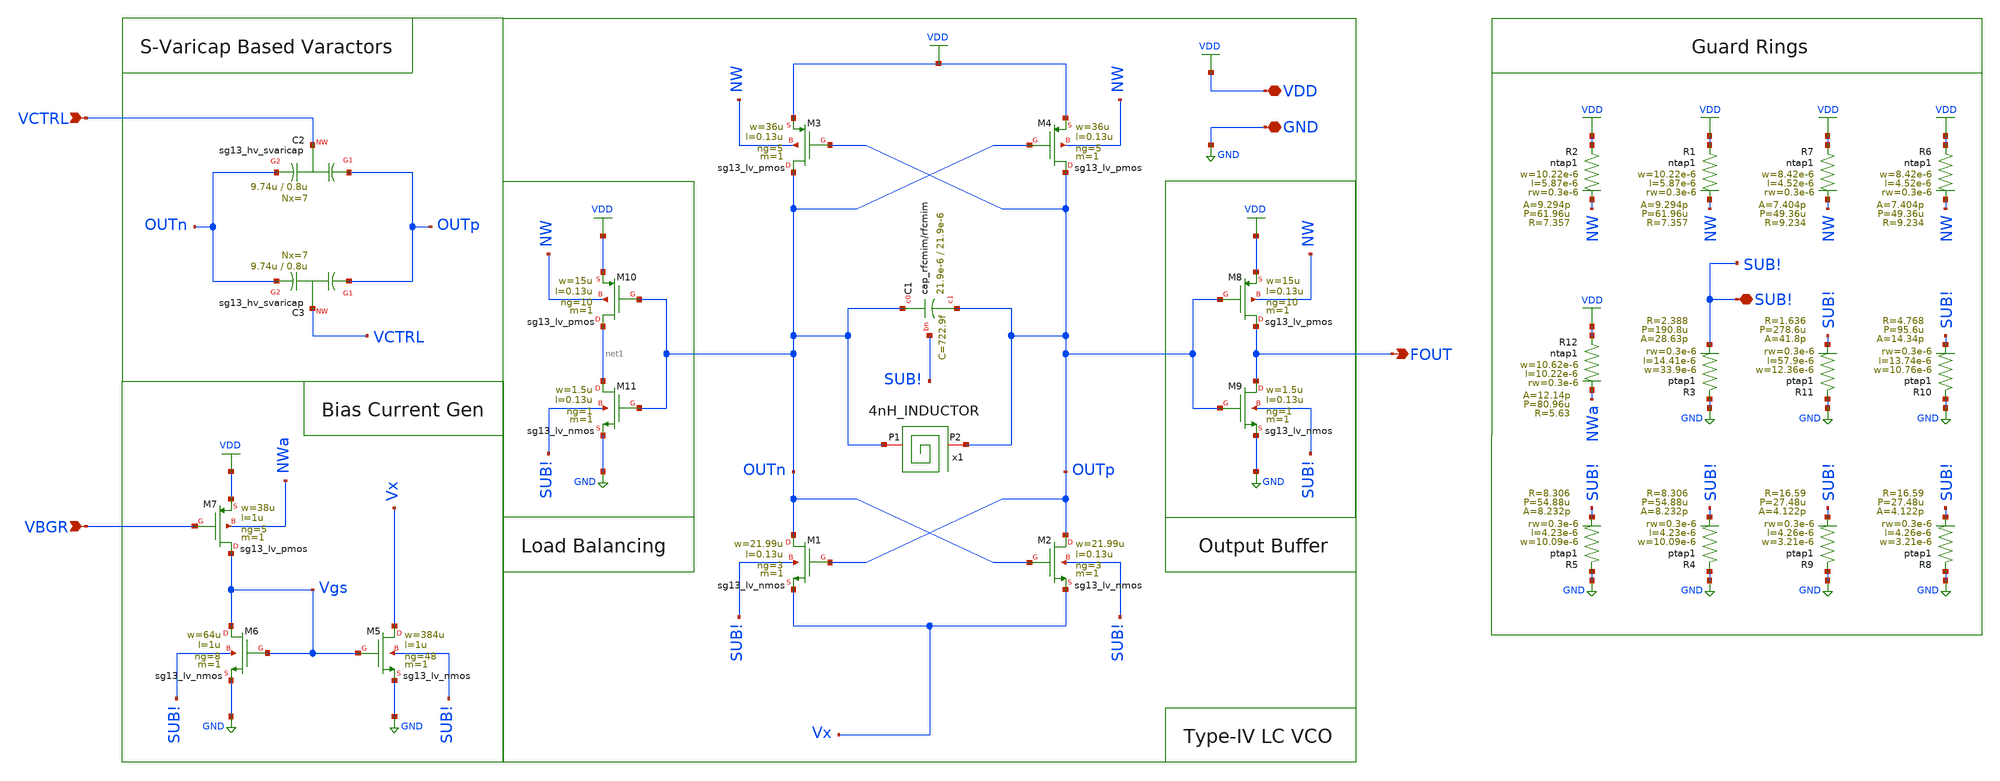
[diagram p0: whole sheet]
** sch_path: xschem/lc-vco/LC_VCO.sch
**.subckt LC_VCO FOUT VCTRL VBGR VDD GND SUB!
*.opin FOUT
*.ipin VCTRL
*.ipin VBGR
*.iopin VDD
*.iopin GND
*.iopin SUB!
x1 OUTn OUTp 4nH_INDUCTOR
XM5 Vx Vgs GND SUB! sg13_lv_nmos w=384u l=1u ng=48 m=1 mm_ok=1
XM4 OUTp OUTn VDD NW sg13_lv_pmos w=36u l=0.13u ng=5 m=1 mm_ok=1
XM3 OUTn OUTp VDD NW sg13_lv_pmos w=36u l=0.13u ng=5 m=1 mm_ok=1
XM2 OUTp OUTn Vx SUB! sg13_lv_nmos w=21.99u l=0.13u ng=3 m=1 mm_ok=1
XM1 OUTn OUTp Vx SUB! sg13_lv_nmos w=21.99u l=0.13u ng=3 m=1 mm_ok=1
XM6 Vgs Vgs GND SUB! sg13_lv_nmos w=64u l=1u ng=8 m=1 mm_ok=1
XC1 OUTn OUTp SUB! cap_rfcmim w=21.9e-6 l=21.9e-6 wfeed=10.0e-6 m=1 mm_ok=1
XC3 OUTp VCTRL OUTn sub! sg13_hv_svaricap w=9.74u l=0.8u Nx=7 mm_ok=1
XC2 OUTp VCTRL OUTn sub! sg13_hv_svaricap w=9.74u l=0.8u Nx=7 mm_ok=1
XM7 Vgs VBGR VDD NWa sg13_lv_pmos w=38u l=1u ng=5 m=1 mm_ok=1
XM8 FOUT OUTp VDD NW sg13_lv_pmos w=15u l=0.13u ng=10 m=1 mm_ok=1
XM9 FOUT OUTp GND SUB! sg13_lv_nmos w=1.5u l=0.13u ng=1 m=1 mm_ok=1
XM10 net1 OUTn VDD NW sg13_lv_pmos w=15u l=0.13u ng=10 m=1 mm_ok=1
XM11 net1 OUTn GND SUB! sg13_lv_nmos w=1.5u l=0.13u ng=1 m=1 mm_ok=1
XR1 VDD NW ntap1 R=7.357 w=10.22e-6 l=5.87e-6 rw=0.3e-6
XR2 VDD NW ntap1 R=7.357 w=10.22e-6 l=5.87e-6 rw=0.3e-6
XR3 GND SUB! ptap1 R=2.388 w=33.9e-6 l=14.41e-6 rw=0.3e-6
XR4 GND SUB! ptap1 R=8.306 w=10.09e-6 l=4.23e-6 rw=0.3e-6
XR5 GND SUB! ptap1 R=8.306 w=10.09e-6 l=4.23e-6 rw=0.3e-6
XR6 VDD NW ntap1 R=9.234 w=8.42e-6 l=4.52e-6 rw=0.3e-6
XR7 VDD NW ntap1 R=9.234 w=8.42e-6 l=4.52e-6 rw=0.3e-6
XR8 GND SUB! ptap1 R=16.59 w=3.21e-6 l=4.26e-6 rw=0.3e-6
XR9 GND SUB! ptap1 R=16.59 w=3.21e-6 l=4.26e-6 rw=0.3e-6
XR10 GND SUB! ptap1 R=4.768 w=10.76e-6 l=13.74e-6 rw=0.3e-6
XR11 GND SUB! ptap1 R=1.636 w=12.36e-6 l=57.9e-6 rw=0.3e-6
XR12 VDD NWa ntap1 R=5.63 w=10.62e-6 l=10.22e-6 rw=0.3e-6
**** begin user architecture code


.subckt 4nH_INDUCTOR 1 2
* LVS black-box stub only
* Full model is available in 4nH_INDUCTOR.spice
.ends


**** end user architecture code
**.ends
.GLOBAL GND
.GLOBAL VDD
.end
